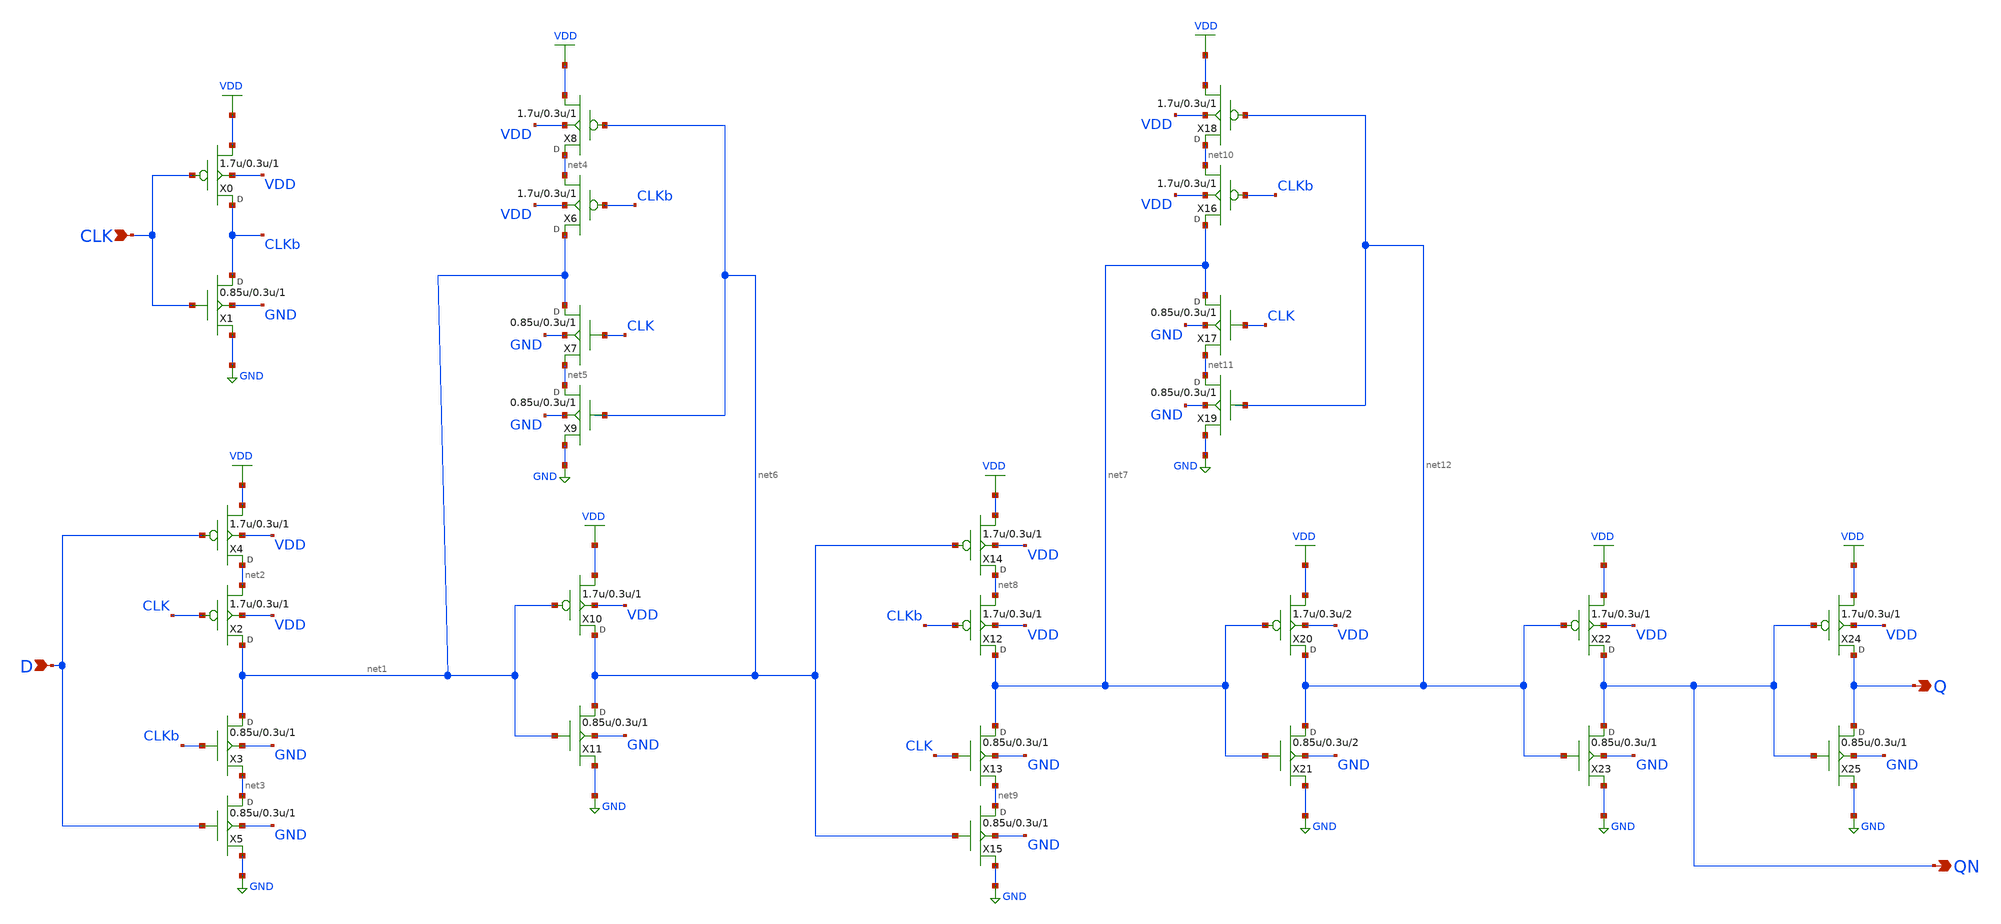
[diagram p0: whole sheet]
** sch_path: lib/xschem/gf180mcu_osu_sc_12T_dff_1.sch
**.subckt gf180mcu_osu_sc_12T_dff_1 CLK D Q QN
*.ipin CLK
*.ipin D
*.opin Q
*.opin QN
X0 CLKb CLK VDD VDD pmos_3p3 w=1.7u l=0.3u m=1
X1 CLKb CLK GND GND nmos_3p3 w=0.85u l=0.3u m=1
X2 net1 CLK net2 VDD pmos_3p3 w=1.7u l=0.3u m=1
X3 net1 CLKb net3 GND nmos_3p3 w=0.85u l=0.3u m=1
X4 net2 D VDD VDD pmos_3p3 w=1.7u l=0.3u m=1
X5 net3 D GND GND nmos_3p3 w=0.85u l=0.3u m=1
X6 net1 CLKb net4 VDD pmos_3p3 w=1.7u l=0.3u m=1
X7 net1 CLK net5 GND nmos_3p3 w=0.85u l=0.3u m=1
X8 net4 net6 VDD VDD pmos_3p3 w=1.7u l=0.3u m=1
X9 net5 net6 GND GND nmos_3p3 w=0.85u l=0.3u m=1
X10 net6 net1 VDD VDD pmos_3p3 w=1.7u l=0.3u m=1
X11 net6 net1 GND GND nmos_3p3 w=0.85u l=0.3u m=1
X12 net7 CLKb net8 VDD pmos_3p3 w=1.7u l=0.3u m=1
X13 net7 CLK net9 GND nmos_3p3 w=0.85u l=0.3u m=1
X14 net8 net6 VDD VDD pmos_3p3 w=1.7u l=0.3u m=1
X15 net9 net6 GND GND nmos_3p3 w=0.85u l=0.3u m=1
X16 net7 CLKb net10 VDD pmos_3p3 w=1.7u l=0.3u m=1
X17 net7 CLK net11 GND nmos_3p3 w=0.85u l=0.3u m=1
X18 net10 net12 VDD VDD pmos_3p3 w=1.7u l=0.3u m=1
X19 net11 net12 GND GND nmos_3p3 w=0.85u l=0.3u m=1
X20 net12 net7 VDD VDD pmos_3p3 w=1.7u l=0.3u m=2
X21 net12 net7 GND GND nmos_3p3 w=0.85u l=0.3u m=2
X22 QN net12 VDD VDD pmos_3p3 w=1.7u l=0.3u m=1
X23 QN net12 GND GND nmos_3p3 w=0.85u l=0.3u m=1
X24 Q QN VDD VDD pmos_3p3 w=1.7u l=0.3u m=1
X25 Q QN GND GND nmos_3p3 w=0.85u l=0.3u m=1
**** begin user architecture code


.inc "/import/yukari1/lrburle/OSU_180/char/techfiles/design.hspice"
.lib "/import/yukari1/lrburle/OSU_180/char/techfiles/sm141064.hspice" typical


**** end user architecture code
**.ends
.GLOBAL VDD
.GLOBAL GND
.end
